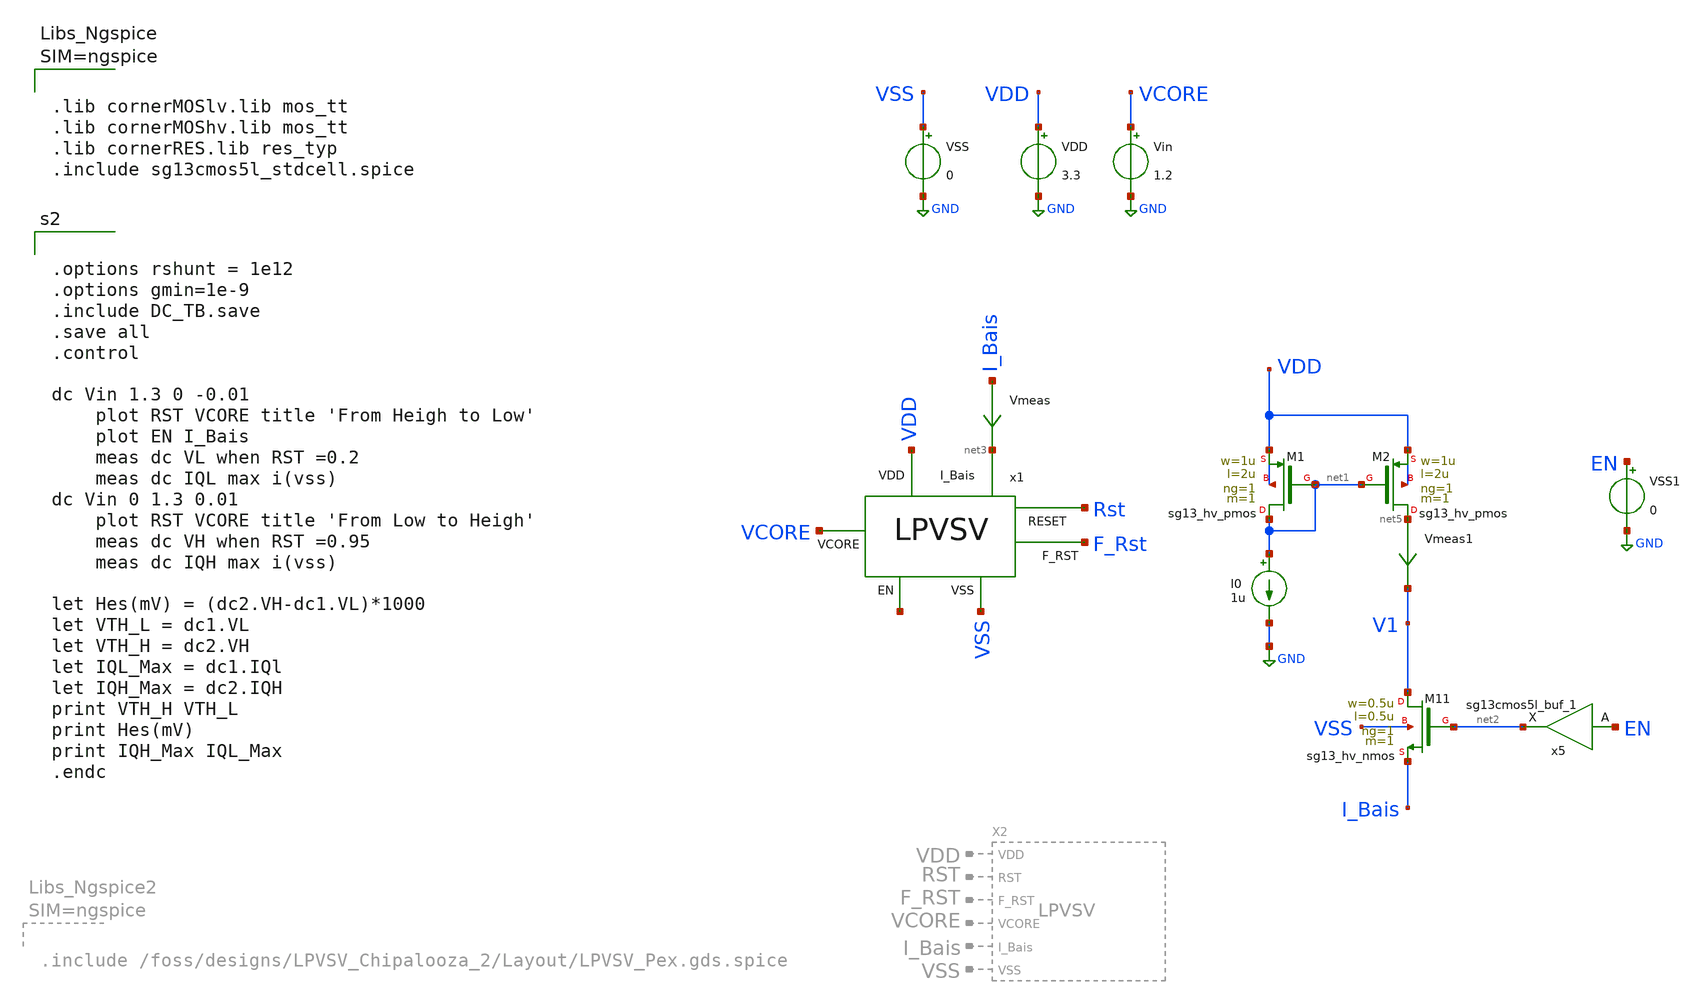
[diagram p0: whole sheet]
** sch_path: Simulation/DC_EN_TB.sch
**.subckt DC_EN_TB
VDD VDD GND 3.3
VSS VSS GND 0
Vin VCORE GND 1.2
x1 VDD VCORE net3 Rst F_Rst VSS net4 LPVSV
VSS1 EN GND 0
Vmeas I_Bais net3 0
.save i(vmeas)
XM11 V1 net2 I_Bais VSS sg13_hv_nmos w=0.5u l=0.5u ng=1 m=1 mm_ok=1
x5 net2 EN V1 VSS sg13cmos5l_buf_1
I0 net1 GND 1u
Vmeas1 net5 V1 0
.save i(vmeas1)
XM1 net1 net1 VDD VDD sg13_hv_pmos w=1u l=2u ng=1 m=1 mm_ok=1
XM2 net5 net1 VDD VDD sg13_hv_pmos w=1u l=2u ng=1 m=1 mm_ok=1
**** begin user architecture code


.options rshunt = 1e12
.options gmin=1e-9
.include DC_TB.save
.save all
.control

dc Vin 1.3 0 -0.01
	plot RST VCORE title 'From Heigh to Low'
	plot EN I_Bais
	meas dc VL when RST =0.2
	meas dc IQL max i(vss)
dc Vin 0 1.3 0.01
	plot RST VCORE title 'From Low to Heigh'
	meas dc VH when RST =0.95
	meas dc IQH max i(vss)

let Hes(mV) = (dc2.VH-dc1.VL)*1000
let VTH_L = dc1.VL
let VTH_H = dc2.VH
let IQL_Max = dc1.IQl
let IQH_Max = dc2.IQH
print VTH_H VTH_L
print Hes(mV)
print IQH_Max IQL_Max
.endc




.options rshunt = 1e15
.options gmin=1e-9
.options reltol = 0.01 abstol = 1p
.option filetype=ascii





.lib cornerMOSlv.lib mos_tt
.lib cornerMOShv.lib mos_tt
.lib cornerRES.lib res_typ
.include sg13cmos5l_stdcell.spice



**** end user architecture code
**.ends
.GLOBAL GND
.end
